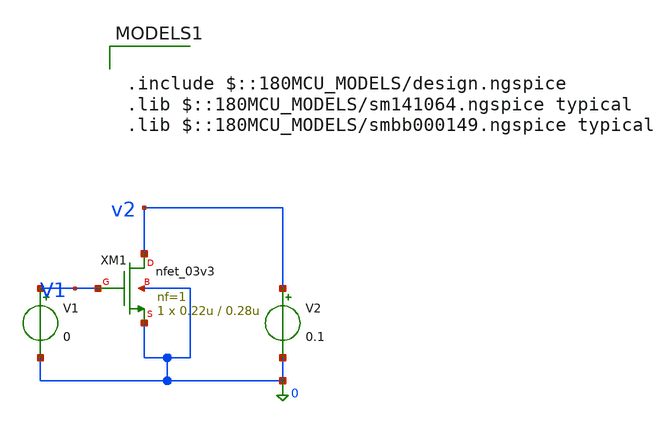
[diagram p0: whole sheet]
** sch_path: src/schematic/KARAKTERISASI/karakterisasi_n3v3.sch
**.subckt karakterisasi_n3v3
XM1 v2 V1 0 0 nfet_03v3 L=0.28u W=0.22u nf=1 ad='int((nf+1)/2) * W/nf * 0.18u' as='int((nf+2)/2) * W/nf * 0.18u'
+ pd='2*int((nf+1)/2) * (W/nf + 0.18u)' ps='2*int((nf+2)/2) * (W/nf + 0.18u)' nrd='0.18u / W' nrs='0.18u / W'
+ sa=0 sb=0 sd=0 m=1
V1 V1 0 0
.save i(v1)
V2 v2 0 0.1
.save i(v2)
**** begin user architecture code

.include $::180MCU_MODELS/design.ngspice
.lib $::180MCU_MODELS/sm141064.ngspice typical
.lib $::180MCU_MODELS/smbb000149.ngspice typical

**** end user architecture code
**.ends
.end
